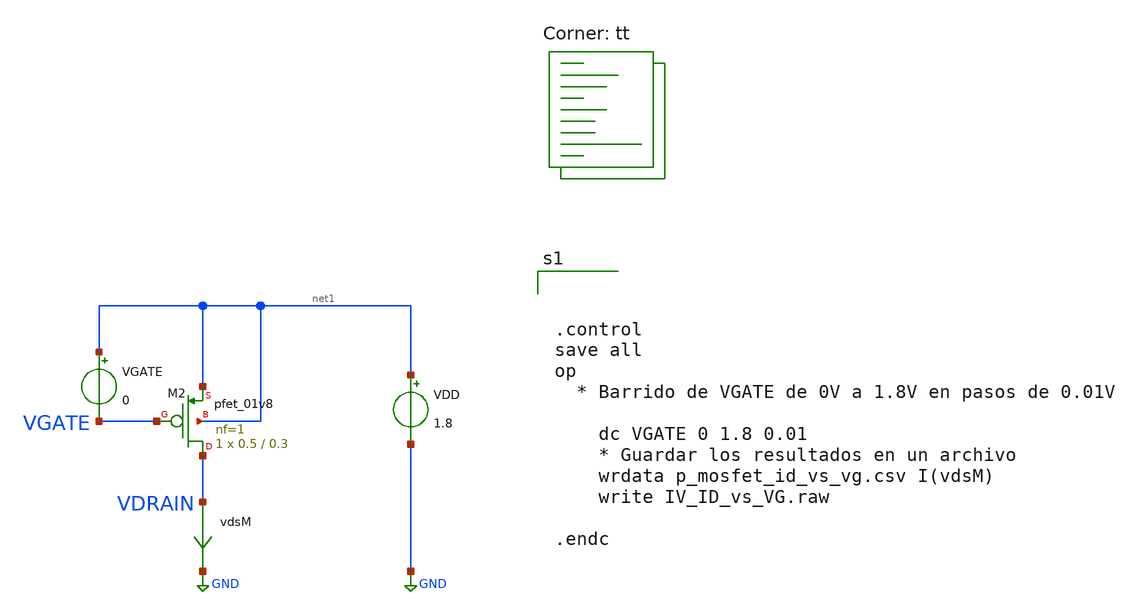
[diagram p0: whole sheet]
** sch_path: circuits/copys_to_develop_pmos/IV_ID_vs_VG.sch
**.subckt IV_ID_vs_VG
VGATE net1 VGATE 0
vdsM VDRAIN GND 0
.save i(vdsm)
XM2 VDRAIN VGATE net1 net1 sky130_fd_pr__pfet_01v8 L=0.3 W=0.5 nf=1 ad='int((nf+1)/2) * W/nf * 0.29'
+ as='int((nf+2)/2) * W/nf * 0.29' pd='2*int((nf+1)/2) * (W/nf + 0.29)' ps='2*int((nf+2)/2) * (W/nf + 0.29)'
+ nrd='0.29 / W' nrs='0.29 / W' sa=0 sb=0 sd=0 mult=1 m=1
VDD net1 GND 1.8
**** begin user architecture code



.control
save all
op
  * Barrido de VGATE de 0V a 1.8V en pasos de 0.01V

    dc VGATE 0 1.8 0.01
    * Guardar los resultados en un archivo
    wrdata p_mosfet_id_vs_vg.csv I(vdsM)
    write IV_ID_vs_VG.raw

.endc



.lib $::SKYWATER_MODELS/sky130.lib.spice tt
**** end user architecture code
**.ends
.GLOBAL GND
.end
